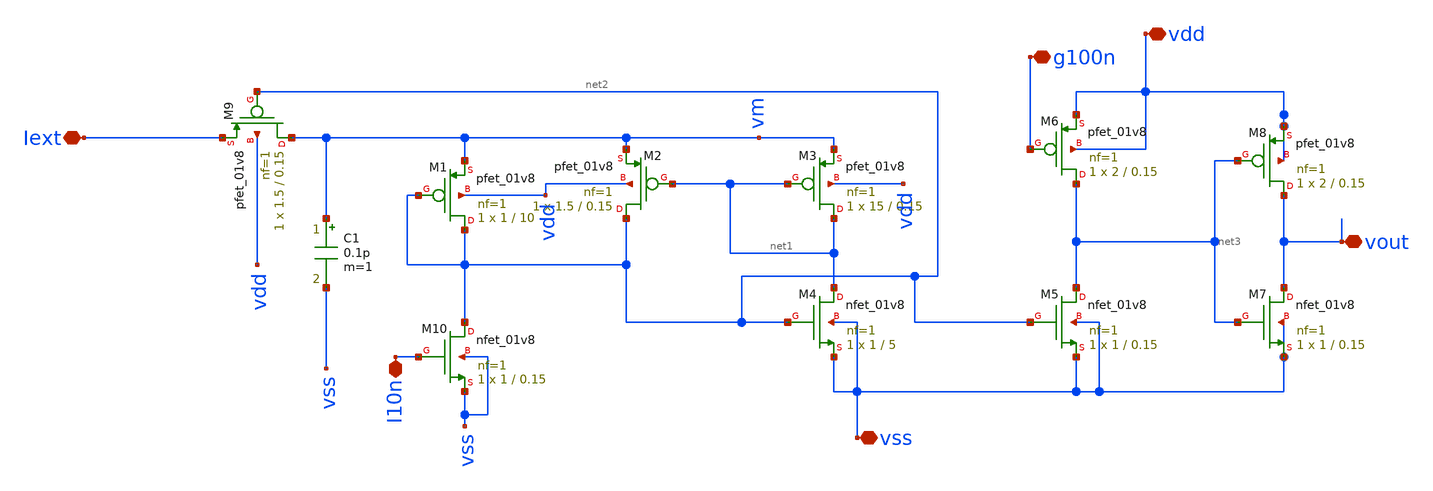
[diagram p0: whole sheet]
** sch_path: Neuron/ultralif/ultralif.sch
**.subckt ultralif Iext vout vss I10n vdd g100n
*.iopin Iext
*.iopin vout
*.iopin vss
*.iopin I10n
*.iopin vdd
*.iopin g100n
XM1 net2 net2 vm vdd sky130_fd_pr__pfet_01v8 L=10 W=1 nf=1 ad='int((nf+1)/2) * W/nf * 0.29' as='int((nf+2)/2) * W/nf * 0.29'
+ pd='2*int((nf+1)/2) * (W/nf + 0.29)' ps='2*int((nf+2)/2) * (W/nf + 0.29)' nrd='0.29 / W' nrs='0.29 / W'
+ sa=0 sb=0 sd=0 mult=1 m=1
XM2 net2 net1 vm vdd sky130_fd_pr__pfet_01v8 L=0.15 W=1.5 nf=1 ad='int((nf+1)/2) * W/nf * 0.29' as='int((nf+2)/2) * W/nf * 0.29'
+ pd='2*int((nf+1)/2) * (W/nf + 0.29)' ps='2*int((nf+2)/2) * (W/nf + 0.29)' nrd='0.29 / W' nrs='0.29 / W'
+ sa=0 sb=0 sd=0 mult=1 m=1
XM3 net1 net1 vm vdd sky130_fd_pr__pfet_01v8 L=0.15 W=15 nf=1 ad='int((nf+1)/2) * W/nf * 0.29' as='int((nf+2)/2) * W/nf * 0.29'
+ pd='2*int((nf+1)/2) * (W/nf + 0.29)' ps='2*int((nf+2)/2) * (W/nf + 0.29)' nrd='0.29 / W' nrs='0.29 / W'
+ sa=0 sb=0 sd=0 mult=1 m=1
XM4 net1 net2 vss vss sky130_fd_pr__nfet_01v8 L=5 W=1 nf=1 ad='int((1 + 1)/2) * 1 / 1 * 0.29' as='int((1 + 2)/2) * 1 / 1 * 0.29'
+ pd='2*int((1 + 1)/2) * (1 / 1 + 0.29)' ps='2*int((1 + 2)/2) * (1 / 1 + 0.29)' nrd='0.29 / 1 ' nrs='0.29 / 1 '
+ sa=0 sb=0 sd=0 mult=1 m=1
C1 vm vss 0.1p m=1
XM10 net2 I10n vss vss sky130_fd_pr__nfet_01v8 L=0.15 W=1 nf=1 ad='int((1 + 1)/2) * 1 / 1 * 0.29' as='int((1 + 2)/2) * 1 / 1 * 0.29'
+ pd='2*int((1 + 1)/2) * (1 / 1 + 0.29)' ps='2*int((1 + 2)/2) * (1 / 1 + 0.29)' nrd='0.29 / 1 ' nrs='0.29 / 1 '
+ sa=0 sb=0 sd=0 mult=1 m=1
XM5 net3 net2 vss vss sky130_fd_pr__nfet_01v8 L=0.15 W=1 nf=1 ad='int((1 + 1)/2) * 1 / 1 * 0.29' as='int((1 + 2)/2) * 1 / 1 * 0.29'
+ pd='2*int((1 + 1)/2) * (1 / 1 + 0.29)' ps='2*int((1 + 2)/2) * (1 / 1 + 0.29)' nrd='0.29 / 1 ' nrs='0.29 / 1 '
+ sa=0 sb=0 sd=0 mult=1 m=1
XM6 net3 g100n vdd vdd sky130_fd_pr__pfet_01v8 L=0.15 W=2 nf=1 ad='int((nf+1)/2) * W/nf * 0.29' as='int((nf+2)/2) * W/nf * 0.29'
+ pd='2*int((nf+1)/2) * (W/nf + 0.29)' ps='2*int((nf+2)/2) * (W/nf + 0.29)' nrd='0.29 / W' nrs='0.29 / W'
+ sa=0 sb=0 sd=0 mult=1 m=1
XM7 vout net3 vss vss sky130_fd_pr__nfet_01v8 L=0.15 W=1 nf=1 ad='int((1 + 1)/2) * 1 / 1 * 0.29' as='int((1 + 2)/2) * 1 / 1 * 0.29'
+ pd='2*int((1 + 1)/2) * (1 / 1 + 0.29)' ps='2*int((1 + 2)/2) * (1 / 1 + 0.29)' nrd='0.29 / 1 ' nrs='0.29 / 1 '
+ sa=0 sb=0 sd=0 mult=1 m=1
XM8 vout net3 vdd vdd sky130_fd_pr__pfet_01v8 L=0.15 W=2 nf=1 ad='int((nf+1)/2) * W/nf * 0.29' as='int((nf+2)/2) * W/nf * 0.29'
+ pd='2*int((nf+1)/2) * (W/nf + 0.29)' ps='2*int((nf+2)/2) * (W/nf + 0.29)' nrd='0.29 / W' nrs='0.29 / W'
+ sa=0 sb=0 sd=0 mult=1 m=1
XM9 vm net2 Iext vdd sky130_fd_pr__pfet_01v8 L=0.15 W=1.5 nf=1 ad='int((nf+1)/2) * W/nf * 0.29' as='int((nf+2)/2) * W/nf * 0.29'
+ pd='2*int((nf+1)/2) * (W/nf + 0.29)' ps='2*int((nf+2)/2) * (W/nf + 0.29)' nrd='0.29 / W' nrs='0.29 / W'
+ sa=0 sb=0 sd=0 mult=1 m=1
**.ends
.end
